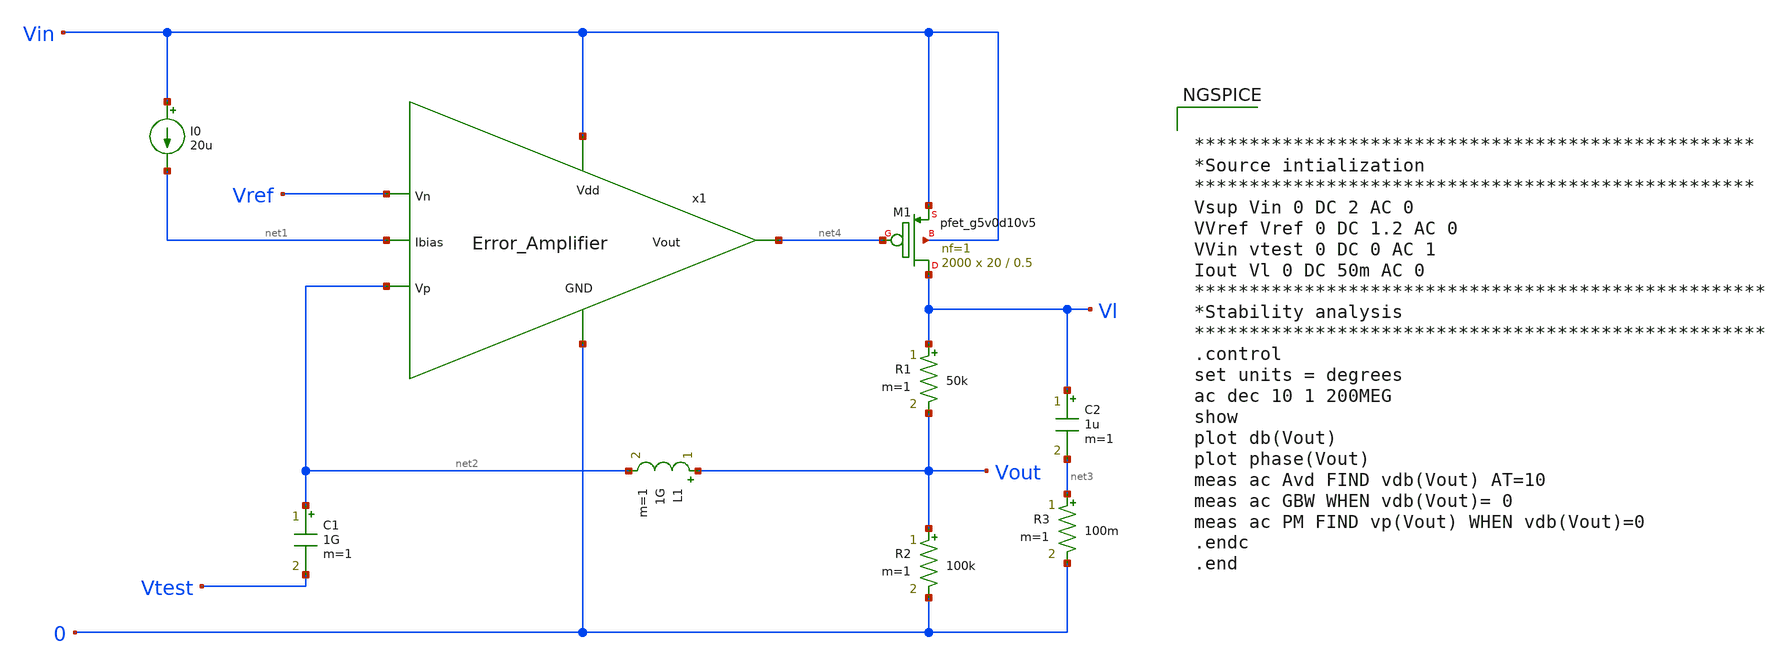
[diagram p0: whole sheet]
** sch_path: Analog_Blocks/LDO/Testbench/LDO_test_stability_TB.sch
**.subckt LDO_test_stability_TB
XM1 Vl net4 Vin Vin sky130_fd_pr__pfet_g5v0d10v5 L=0.5 W=20 nf=1 ad='int((nf+1)/2) * W/nf * 0.29' as='int((nf+2)/2) * W/nf * 0.29'
+ pd='2*int((nf+1)/2) * (W/nf + 0.29)' ps='2*int((nf+2)/2) * (W/nf + 0.29)' nrd='0.29 / W' nrs='0.29 / W'
+ sa=0 sb=0 sd=0 mult=2000 m=2000
R1 Vl Vout 50k m=1
R2 Vout 0 100k m=1
I0 Vin net1 20u
L1 Vout net2 1G m=1
C1 net2 Vtest 1G m=1
C2 Vl net3 1u m=1
R3 net3 0 100m m=1
x1 Vin Vref net2 net4 net1 0 Error_Amplifier
**** begin user architecture code


***************************************************
*Source intialization
***************************************************
Vsup Vin 0 DC 2 AC 0
VVref Vref 0 DC 1.2 AC 0
VVin vtest 0 DC 0 AC 1
Iout Vl 0 DC 50m AC 0
****************************************************
*Stability analysis
****************************************************
.control
set units = degrees
ac dec 10 1 200MEG
show
plot db(Vout)
plot phase(Vout)
meas ac Avd FIND vdb(Vout) AT=10
meas ac GBW WHEN vdb(Vout)= 0
meas ac PM FIND vp(Vout) WHEN vdb(Vout)=0
.endc
.end




.param mc_mm_switch=0
.param mc_pr_switch=0
.include ~/mabrains/pdks/sky130A/libs.ref/sky130_fd_pr/spice/sky130_fd_pr__nfet_01v8__tt.corner.spice
.include ~/mabrains/pdks/sky130A/libs.ref/sky130_fd_pr/spice/sky130_fd_pr__nfet_01v8_lvt__tt.corner.spice
.include ~/mabrains/pdks/sky130A/libs.ref/sky130_fd_pr/spice/sky130_fd_pr__pfet_01v8__tt.corner.spice
.include ~/mabrains/pdks/sky130A/libs.ref/sky130_fd_pr/spice/sky130_fd_pr__nfet_03v3_nvt__tt.corner.spice
.include ~/mabrains/pdks/sky130A/libs.ref/sky130_fd_pr/spice/sky130_fd_pr__nfet_05v0_nvt__tt.corner.spice
.include ~/mabrains/pdks/sky130A/libs.ref/sky130_fd_pr/spice/sky130_fd_pr__esd_nfet_01v8__tt.corner.spice
.include ~/mabrains/pdks/sky130A/libs.ref/sky130_fd_pr/spice/sky130_fd_pr__pfet_01v8_lvt__tt.corner.spice
.include ~/mabrains/pdks/sky130A/libs.ref/sky130_fd_pr/spice/sky130_fd_pr__pfet_01v8_hvt__tt.corner.spice
.include ~/mabrains/pdks/sky130A/libs.ref/sky130_fd_pr/spice/sky130_fd_pr__esd_pfet_g5v0d10v5__tt.corner.spice
.include ~/mabrains/pdks/sky130A/libs.ref/sky130_fd_pr/spice/sky130_fd_pr__pfet_g5v0d10v5__tt.corner.spice
.include ~/mabrains/pdks/sky130A/libs.ref/sky130_fd_pr/spice/sky130_fd_pr__pfet_g5v0d16v0__tt.corner.spice
.include ~/mabrains/pdks/sky130A/libs.ref/sky130_fd_pr/spice/sky130_fd_pr__nfet_g5v0d10v5__tt.corner.spice
.include ~/mabrains/pdks/sky130A/libs.ref/sky130_fd_pr/spice/sky130_fd_pr__nfet_g5v0d16v0__tt_discrete.corner.spice
.include ~/mabrains/pdks/sky130A/libs.ref/sky130_fd_pr/spice/sky130_fd_pr__esd_nfet_g5v0d10v5__tt.corner.spice
.include ~/mabrains/pdks/sky130A/libs.tech/ngspice/corners/tt/nonfet.spice
* Mismatch parameters
.include ~/mabrains/pdks/sky130A/libs.ref/sky130_fd_pr/spice/sky130_fd_pr__nfet_01v8__mismatch.corner.spice
.include ~/mabrains/pdks/sky130A/libs.ref/sky130_fd_pr/spice/sky130_fd_pr__pfet_01v8__mismatch.corner.spice
.include ~/mabrains/pdks/sky130A/libs.ref/sky130_fd_pr/spice/sky130_fd_pr__nfet_01v8_lvt__mismatch.corner.spice
.include ~/mabrains/pdks/sky130A/libs.ref/sky130_fd_pr/spice/sky130_fd_pr__pfet_01v8_lvt__mismatch.corner.spice
.include ~/mabrains/pdks/sky130A/libs.ref/sky130_fd_pr/spice/sky130_fd_pr__pfet_01v8_hvt__mismatch.corner.spice
.include ~/mabrains/pdks/sky130A/libs.ref/sky130_fd_pr/spice/sky130_fd_pr__nfet_g5v0d10v5__mismatch.corner.spice
.include ~/mabrains/pdks/sky130A/libs.ref/sky130_fd_pr/spice/sky130_fd_pr__pfet_g5v0d10v5__mismatch.corner.spice
.include ~/mabrains/pdks/sky130A/libs.ref/sky130_fd_pr/spice/sky130_fd_pr__nfet_05v0_nvt__mismatch.corner.spice
.include ~/mabrains/pdks/sky130A/libs.ref/sky130_fd_pr/spice/sky130_fd_pr__nfet_03v3_nvt__mismatch.corner.spice
* Resistor/Capacitor
.include ~/mabrains/pdks/sky130A/libs.tech/ngspice/r+c/res_typical__cap_typical.spice
.include ~/mabrains/pdks/sky130A/libs.tech/ngspice/r+c/res_typical__cap_typical__lin.spice
* Special cells
.include ~/mabrains/pdks/sky130A/libs.tech/ngspice/corners/tt/specialized_cells.spice
* All models
.include ~/mabrains/pdks/sky130A/libs.tech/ngspice/all.spice
* Corner
.include ~/mabrains/pdks/sky130A/libs.tech/ngspice/corners/tt/rf.spice



**** end user architecture code
**.ends
.end
